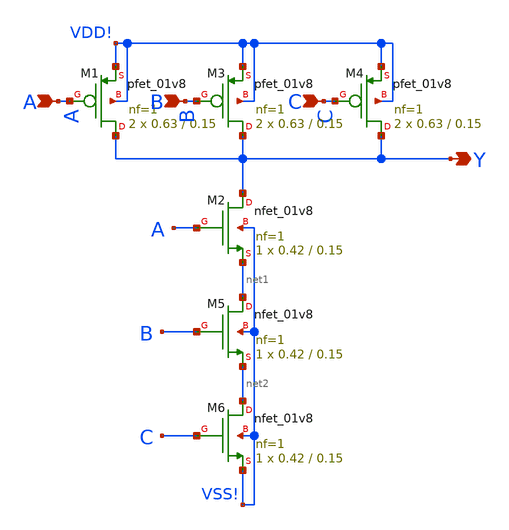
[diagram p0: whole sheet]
** sch_path: 3_nand1X/3_nand1X.sch
**.subckt 3_nand1X A B C Y
*.ipin A
*.ipin B
*.ipin C
*.opin Y
XM1 Y A VDD! VDD! sky130_fd_pr__pfet_01v8 L=0.15 W=0.63 nf=1 ad='int((1 + 1)/2) * 0.63 / 1 * 0.29' as='int((1 + 2)/2) * 0.63 / 1 * 0.29'
+ pd='2*int((1 + 1)/2) * (0.63 / 1 + 0.29)' ps='2*int((1 + 2)/2) * (0.63 / 1 + 0.29)' nrd='0.29 / 0.63 '
+ nrs='0.29 / 0.63 ' sa=0 sb=0 sd=0 mult=2 m=2
XM2 Y A net1 VSS! sky130_fd_pr__nfet_01v8 L=0.15 W=0.42 nf=1 ad='int((1 + 1)/2) * 0.42 / 1 * 0.29' as='int((1 + 2)/2) * 0.42 / 1 * 0.29'
+ pd='2*int((1 + 1)/2) * (0.42 / 1 + 0.29)' ps='2*int((1 + 2)/2) * (0.42 / 1 + 0.29)' nrd='0.29 / 0.42 '
+ nrs='0.29 / 0.42 ' sa=0 sb=0 sd=0 mult=1 m=1
XM5 net1 B net2 VSS! sky130_fd_pr__nfet_01v8 L=0.15 W=0.42 nf=1 ad='int((1 + 1)/2) * 0.42 / 1 * 0.29'
+ as='int((1 + 2)/2) * 0.42 / 1 * 0.29' pd='2*int((1 + 1)/2) * (0.42 / 1 + 0.29)' ps='2*int((1 + 2)/2) * (0.42 / 1 + 0.29)'
+ nrd='0.29 / 0.42 ' nrs='0.29 / 0.42 ' sa=0 sb=0 sd=0 mult=1 m=1
XM6 net2 C VSS! VSS! sky130_fd_pr__nfet_01v8 L=0.15 W=0.42 nf=1 ad='int((1 + 1)/2) * 0.42 / 1 * 0.29'
+ as='int((1 + 2)/2) * 0.42 / 1 * 0.29' pd='2*int((1 + 1)/2) * (0.42 / 1 + 0.29)' ps='2*int((1 + 2)/2) * (0.42 / 1 + 0.29)'
+ nrd='0.29 / 0.42 ' nrs='0.29 / 0.42 ' sa=0 sb=0 sd=0 mult=1 m=1
XM3 Y B VDD! VDD! sky130_fd_pr__pfet_01v8 L=0.15 W=0.63 nf=1 ad='int((1 + 1)/2) * 0.63 / 1 * 0.29' as='int((1 + 2)/2) * 0.63 / 1 * 0.29'
+ pd='2*int((1 + 1)/2) * (0.63 / 1 + 0.29)' ps='2*int((1 + 2)/2) * (0.63 / 1 + 0.29)' nrd='0.29 / 0.63 '
+ nrs='0.29 / 0.63 ' sa=0 sb=0 sd=0 mult=2 m=2
XM4 Y C VDD! VDD! sky130_fd_pr__pfet_01v8 L=0.15 W=0.63 nf=1 ad='int((1 + 1)/2) * 0.63 / 1 * 0.29' as='int((1 + 2)/2) * 0.63 / 1 * 0.29'
+ pd='2*int((1 + 1)/2) * (0.63 / 1 + 0.29)' ps='2*int((1 + 2)/2) * (0.63 / 1 + 0.29)' nrd='0.29 / 0.63 '
+ nrs='0.29 / 0.63 ' sa=0 sb=0 sd=0 mult=2 m=2
**.ends
.end
